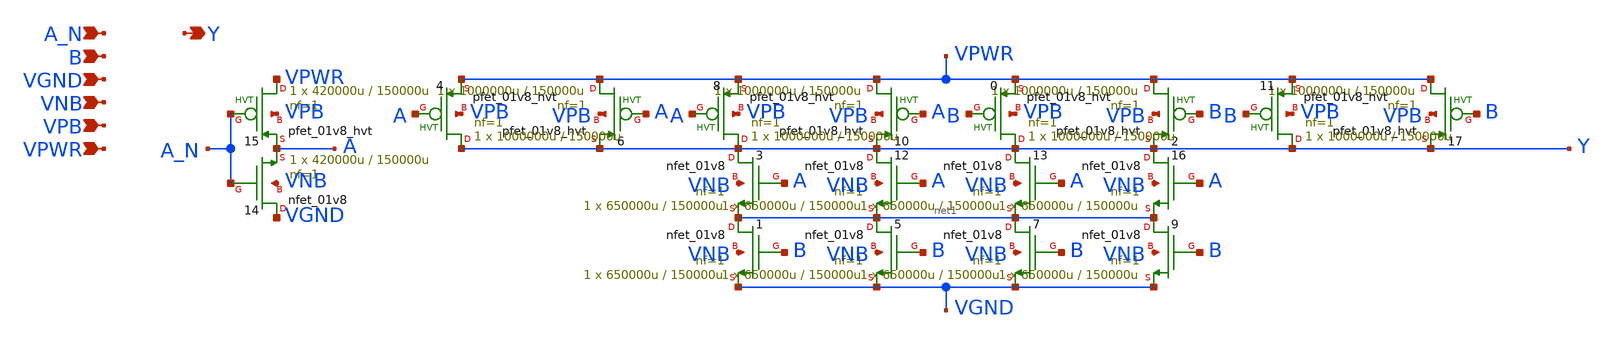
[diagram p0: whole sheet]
** sch_path: schematics/nand2b/sky130_fd_sc_hd__nand2b_4.sch
**.subckt sky130_fd_sc_hd__nand2b_4 A_N B VGND VNB VPB VPWR Y
*.ipin A_N
*.ipin B
*.ipin VGND
*.ipin VNB
*.ipin VPB
*.ipin VPWR
*.opin Y
X6 VPWR A Y VPB sky130_fd_pr__pfet_01v8_hvt L=150000u W=1000000u nf=1 ad='int((1 + 1)/2) * 1000000u / 1 * 0.29'
+ as='int((1 + 2)/2) * 1000000u / 1 * 0.29' pd='2*int((1 + 1)/2) * (1000000u / 1 + 0.29)' ps='2*int((1 + 2)/2) * (1000000u / 1 + 0.29)'
+ nrd='0.29 / 1000000u ' nrs='0.29 / 1000000u ' sa=0 sb=0 sd=0 mult=1 m=1
X4 Y A VPWR VPB sky130_fd_pr__pfet_01v8_hvt L=150000u W=1000000u nf=1 ad='int((1 + 1)/2) * 1000000u / 1 * 0.29'
+ as='int((1 + 2)/2) * 1000000u / 1 * 0.29' pd='2*int((1 + 1)/2) * (1000000u / 1 + 0.29)' ps='2*int((1 + 2)/2) * (1000000u / 1 + 0.29)'
+ nrd='0.29 / 1000000u ' nrs='0.29 / 1000000u ' sa=0 sb=0 sd=0 mult=1 m=1
X3 Y A net1 VNB sky130_fd_pr__nfet_01v8 L=150000u W=650000u nf=1 ad='int((1 + 1)/2) * 650000u / 1 * 0.29'
+ as='int((1 + 2)/2) * 650000u / 1 * 0.29' pd='2*int((1 + 1)/2) * (650000u / 1 + 0.29)' ps='2*int((1 + 2)/2) * (650000u / 1 + 0.29)'
+ nrd='0.29 / 650000u ' nrs='0.29 / 650000u ' sa=0 sb=0 sd=0 mult=1 m=1
X1 net1 B VGND VNB sky130_fd_pr__nfet_01v8 L=150000u W=650000u nf=1 ad='int((1 + 1)/2) * 650000u / 1 * 0.29'
+ as='int((1 + 2)/2) * 650000u / 1 * 0.29' pd='2*int((1 + 1)/2) * (650000u / 1 + 0.29)' ps='2*int((1 + 2)/2) * (650000u / 1 + 0.29)'
+ nrd='0.29 / 650000u ' nrs='0.29 / 650000u ' sa=0 sb=0 sd=0 mult=1 m=1
X14 VGND A_N A VNB sky130_fd_pr__nfet_01v8 L=150000u W=420000u nf=1 ad='int((1 + 1)/2) * 420000u / 1 * 0.29'
+ as='int((1 + 2)/2) * 420000u / 1 * 0.29' pd='2*int((1 + 1)/2) * (420000u / 1 + 0.29)' ps='2*int((1 + 2)/2) * (420000u / 1 + 0.29)'
+ nrd='0.29 / 420000u ' nrs='0.29 / 420000u ' sa=0 sb=0 sd=0 mult=1 m=1
X15 VPWR A_N A VPB sky130_fd_pr__pfet_01v8_hvt L=150000u W=420000u nf=1 ad='int((1 + 1)/2) * 420000u / 1 * 0.29'
+ as='int((1 + 2)/2) * 420000u / 1 * 0.29' pd='2*int((1 + 1)/2) * (420000u / 1 + 0.29)' ps='2*int((1 + 2)/2) * (420000u / 1 + 0.29)'
+ nrd='0.29 / 420000u ' nrs='0.29 / 420000u ' sa=0 sb=0 sd=0 mult=1 m=1
X12 Y A net1 VNB sky130_fd_pr__nfet_01v8 L=150000u W=650000u nf=1 ad='int((1 + 1)/2) * 650000u / 1 * 0.29'
+ as='int((1 + 2)/2) * 650000u / 1 * 0.29' pd='2*int((1 + 1)/2) * (650000u / 1 + 0.29)' ps='2*int((1 + 2)/2) * (650000u / 1 + 0.29)'
+ nrd='0.29 / 650000u ' nrs='0.29 / 650000u ' sa=0 sb=0 sd=0 mult=1 m=1
X5 net1 B VGND VNB sky130_fd_pr__nfet_01v8 L=150000u W=650000u nf=1 ad='int((1 + 1)/2) * 650000u / 1 * 0.29'
+ as='int((1 + 2)/2) * 650000u / 1 * 0.29' pd='2*int((1 + 1)/2) * (650000u / 1 + 0.29)' ps='2*int((1 + 2)/2) * (650000u / 1 + 0.29)'
+ nrd='0.29 / 650000u ' nrs='0.29 / 650000u ' sa=0 sb=0 sd=0 mult=1 m=1
X17 VPWR B Y VPB sky130_fd_pr__pfet_01v8_hvt L=150000u W=1000000u nf=1 ad='int((1 + 1)/2) * 1000000u / 1 * 0.29'
+ as='int((1 + 2)/2) * 1000000u / 1 * 0.29' pd='2*int((1 + 1)/2) * (1000000u / 1 + 0.29)' ps='2*int((1 + 2)/2) * (1000000u / 1 + 0.29)'
+ nrd='0.29 / 1000000u ' nrs='0.29 / 1000000u ' sa=0 sb=0 sd=0 mult=1 m=1
X11 Y B VPWR VPB sky130_fd_pr__pfet_01v8_hvt L=150000u W=1000000u nf=1 ad='int((1 + 1)/2) * 1000000u / 1 * 0.29'
+ as='int((1 + 2)/2) * 1000000u / 1 * 0.29' pd='2*int((1 + 1)/2) * (1000000u / 1 + 0.29)' ps='2*int((1 + 2)/2) * (1000000u / 1 + 0.29)'
+ nrd='0.29 / 1000000u ' nrs='0.29 / 1000000u ' sa=0 sb=0 sd=0 mult=1 m=1
X13 Y A net1 VNB sky130_fd_pr__nfet_01v8 L=150000u W=650000u nf=1 ad='int((1 + 1)/2) * 650000u / 1 * 0.29'
+ as='int((1 + 2)/2) * 650000u / 1 * 0.29' pd='2*int((1 + 1)/2) * (650000u / 1 + 0.29)' ps='2*int((1 + 2)/2) * (650000u / 1 + 0.29)'
+ nrd='0.29 / 650000u ' nrs='0.29 / 650000u ' sa=0 sb=0 sd=0 mult=1 m=1
X7 net1 B VGND VNB sky130_fd_pr__nfet_01v8 L=150000u W=650000u nf=1 ad='int((1 + 1)/2) * 650000u / 1 * 0.29'
+ as='int((1 + 2)/2) * 650000u / 1 * 0.29' pd='2*int((1 + 1)/2) * (650000u / 1 + 0.29)' ps='2*int((1 + 2)/2) * (650000u / 1 + 0.29)'
+ nrd='0.29 / 650000u ' nrs='0.29 / 650000u ' sa=0 sb=0 sd=0 mult=1 m=1
X16 Y A net1 VNB sky130_fd_pr__nfet_01v8 L=150000u W=650000u nf=1 ad='int((1 + 1)/2) * 650000u / 1 * 0.29'
+ as='int((1 + 2)/2) * 650000u / 1 * 0.29' pd='2*int((1 + 1)/2) * (650000u / 1 + 0.29)' ps='2*int((1 + 2)/2) * (650000u / 1 + 0.29)'
+ nrd='0.29 / 650000u ' nrs='0.29 / 650000u ' sa=0 sb=0 sd=0 mult=1 m=1
X9 net1 B VGND VNB sky130_fd_pr__nfet_01v8 L=150000u W=650000u nf=1 ad='int((1 + 1)/2) * 650000u / 1 * 0.29'
+ as='int((1 + 2)/2) * 650000u / 1 * 0.29' pd='2*int((1 + 1)/2) * (650000u / 1 + 0.29)' ps='2*int((1 + 2)/2) * (650000u / 1 + 0.29)'
+ nrd='0.29 / 650000u ' nrs='0.29 / 650000u ' sa=0 sb=0 sd=0 mult=1 m=1
X10 VPWR A Y VPB sky130_fd_pr__pfet_01v8_hvt L=150000u W=1000000u nf=1 ad='int((1 + 1)/2) * 1000000u / 1 * 0.29'
+ as='int((1 + 2)/2) * 1000000u / 1 * 0.29' pd='2*int((1 + 1)/2) * (1000000u / 1 + 0.29)' ps='2*int((1 + 2)/2) * (1000000u / 1 + 0.29)'
+ nrd='0.29 / 1000000u ' nrs='0.29 / 1000000u ' sa=0 sb=0 sd=0 mult=1 m=1
X8 Y A VPWR VPB sky130_fd_pr__pfet_01v8_hvt L=150000u W=1000000u nf=1 ad='int((1 + 1)/2) * 1000000u / 1 * 0.29'
+ as='int((1 + 2)/2) * 1000000u / 1 * 0.29' pd='2*int((1 + 1)/2) * (1000000u / 1 + 0.29)' ps='2*int((1 + 2)/2) * (1000000u / 1 + 0.29)'
+ nrd='0.29 / 1000000u ' nrs='0.29 / 1000000u ' sa=0 sb=0 sd=0 mult=1 m=1
X2 VPWR B Y VPB sky130_fd_pr__pfet_01v8_hvt L=150000u W=1000000u nf=1 ad='int((1 + 1)/2) * 1000000u / 1 * 0.29'
+ as='int((1 + 2)/2) * 1000000u / 1 * 0.29' pd='2*int((1 + 1)/2) * (1000000u / 1 + 0.29)' ps='2*int((1 + 2)/2) * (1000000u / 1 + 0.29)'
+ nrd='0.29 / 1000000u ' nrs='0.29 / 1000000u ' sa=0 sb=0 sd=0 mult=1 m=1
X0 Y B VPWR VPB sky130_fd_pr__pfet_01v8_hvt L=150000u W=1000000u nf=1 ad='int((1 + 1)/2) * 1000000u / 1 * 0.29'
+ as='int((1 + 2)/2) * 1000000u / 1 * 0.29' pd='2*int((1 + 1)/2) * (1000000u / 1 + 0.29)' ps='2*int((1 + 2)/2) * (1000000u / 1 + 0.29)'
+ nrd='0.29 / 1000000u ' nrs='0.29 / 1000000u ' sa=0 sb=0 sd=0 mult=1 m=1
**.ends
.end
